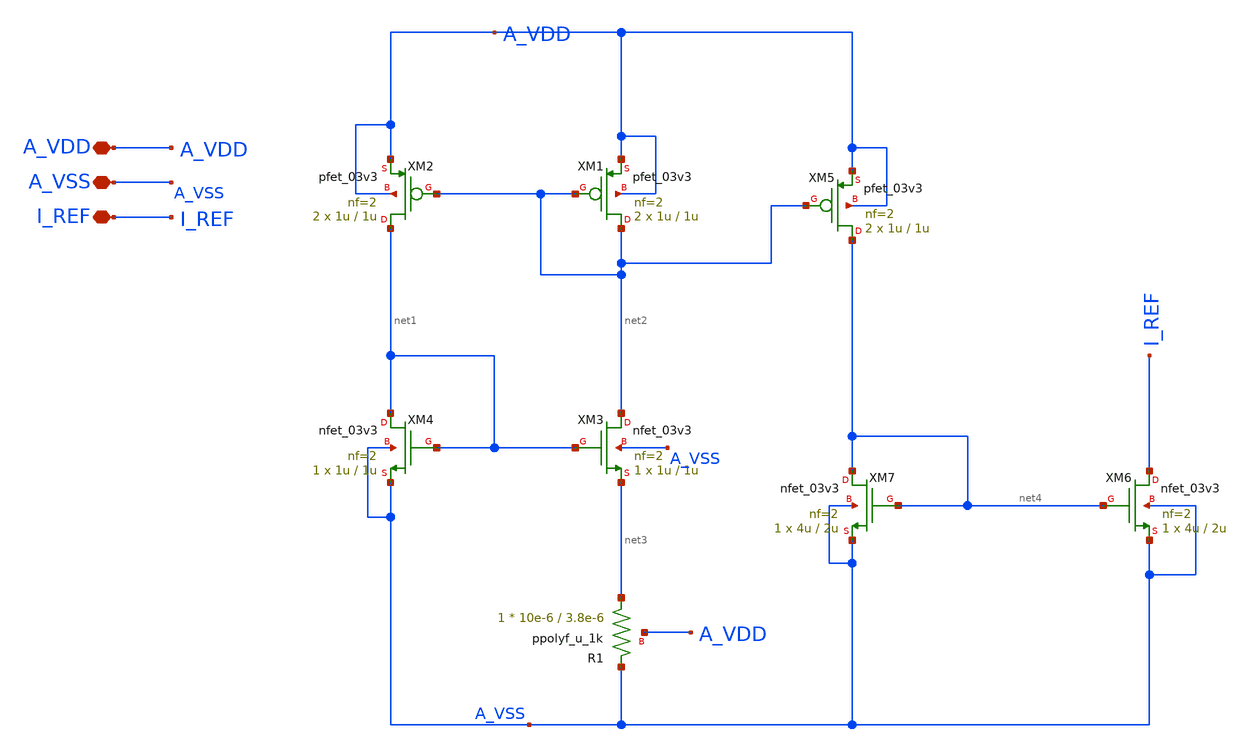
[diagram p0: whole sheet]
** sch_path: designs/libs/TIA/CORE_IREF.sch
**.subckt CORE_IREF I_REF A_VSS A_VDD
*.iopin I_REF
*.iopin A_VSS
*.iopin A_VDD
XM1 net2 net2 A_VDD A_VDD pfet_03v3 L=1u W=1u nf=2 ad='int((nf+1)/2) * W/nf * 0.18u' as='int((nf+2)/2) * W/nf * 0.18u'
+ pd='2*int((nf+1)/2) * (W/nf + 0.18u)' ps='2*int((nf+2)/2) * (W/nf + 0.18u)' nrd='0.18u / W' nrs='0.18u / W'
+ sa=0 sb=0 sd=0 m=2
XM2 net1 net2 A_VDD A_VDD pfet_03v3 L=1u W=1u nf=2 ad='int((nf+1)/2) * W/nf * 0.18u' as='int((nf+2)/2) * W/nf * 0.18u'
+ pd='2*int((nf+1)/2) * (W/nf + 0.18u)' ps='2*int((nf+2)/2) * (W/nf + 0.18u)' nrd='0.18u / W' nrs='0.18u / W'
+ sa=0 sb=0 sd=0 m=2
XM3 net2 net1 net3 A_VSS nfet_03v3 L=1u W=1u nf=2 ad='int((nf+1)/2) * W/nf * 0.18u' as='int((nf+2)/2) * W/nf * 0.18u'
+ pd='2*int((nf+1)/2) * (W/nf + 0.18u)' ps='2*int((nf+2)/2) * (W/nf + 0.18u)' nrd='0.18u / W' nrs='0.18u / W'
+ sa=0 sb=0 sd=0 m=1
XM4 net1 net1 A_VSS A_VSS nfet_03v3 L=1u W=1u nf=2 ad='int((nf+1)/2) * W/nf * 0.18u' as='int((nf+2)/2) * W/nf * 0.18u'
+ pd='2*int((nf+1)/2) * (W/nf + 0.18u)' ps='2*int((nf+2)/2) * (W/nf + 0.18u)' nrd='0.18u / W' nrs='0.18u / W'
+ sa=0 sb=0 sd=0 m=1
XR1 net3 A_VSS A_VDD ppolyf_u_1k r_width=10e-6 r_length=3.8e-6 m=1
XM6 I_REF net4 A_VSS A_VSS nfet_03v3 L=2u W=4u nf=2 ad='int((nf+1)/2) * W/nf * 0.18u' as='int((nf+2)/2) * W/nf * 0.18u'
+ pd='2*int((nf+1)/2) * (W/nf + 0.18u)' ps='2*int((nf+2)/2) * (W/nf + 0.18u)' nrd='0.18u / W' nrs='0.18u / W'
+ sa=0 sb=0 sd=0 m=1
XM7 net4 net4 A_VSS A_VSS nfet_03v3 L=2u W=4u nf=2 ad='int((nf+1)/2) * W/nf * 0.18u' as='int((nf+2)/2) * W/nf * 0.18u'
+ pd='2*int((nf+1)/2) * (W/nf + 0.18u)' ps='2*int((nf+2)/2) * (W/nf + 0.18u)' nrd='0.18u / W' nrs='0.18u / W'
+ sa=0 sb=0 sd=0 m=1
XM5 net4 net2 A_VDD A_VDD pfet_03v3 L=1u W=1u nf=2 ad='int((nf+1)/2) * W/nf * 0.18u' as='int((nf+2)/2) * W/nf * 0.18u'
+ pd='2*int((nf+1)/2) * (W/nf + 0.18u)' ps='2*int((nf+2)/2) * (W/nf + 0.18u)' nrd='0.18u / W' nrs='0.18u / W'
+ sa=0 sb=0 sd=0 m=2
**.ends
.end
